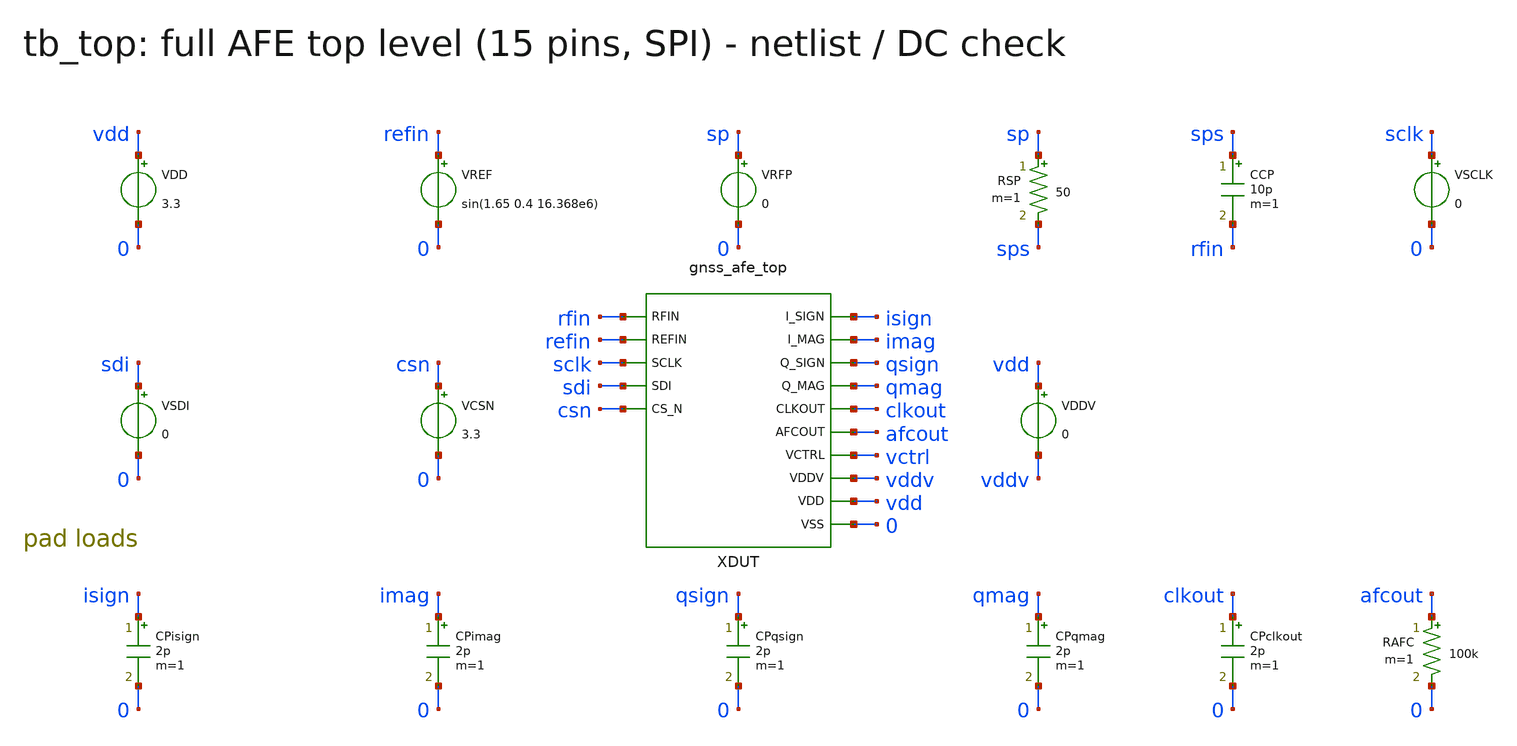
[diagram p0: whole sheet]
** sch_path: v1_claude/xschem/tb_top.sch
**.subckt tb_top
VDD vdd 0 3.3
VREF refin 0 sin(1.65 0.4 16.368e6)
VRFP sp 0 0
RSP sp sps 50 m=1
CCP sps rfin 10p m=1
VSCLK sclk 0 0
VSDI sdi 0 0
VCSN csn 0 3.3
XDUT rfin refin sclk sdi csn isign imag qsign qmag clkout afcout vctrl vddv vdd 0 gnss_afe_top
VDDV vdd vddv 0
CPisign isign 0 2p m=1
CPimag imag 0 2p m=1
CPqsign qsign 0 2p m=1
CPqmag qmag 0 2p m=1
CPclkout clkout 0 2p m=1
RAFC afcout 0 100k m=1
**** begin user architecture code
 .include $::180MCU_MODELS/design.ngspice
.lib $::180MCU_MODELS/sm141064.ngspice typical
.lib $::180MCU_MODELS/sm141064.ngspice res_typical
.lib $::180MCU_MODELS/sm141064.ngspice mimcap_typical

.control
set num_threads=1
op
echo RES idd_total=$&i(VDD) vctrl=$&v(vctrl) afcout=$&v(afcout)
.endc

**** end user architecture code
**.ends
.end
